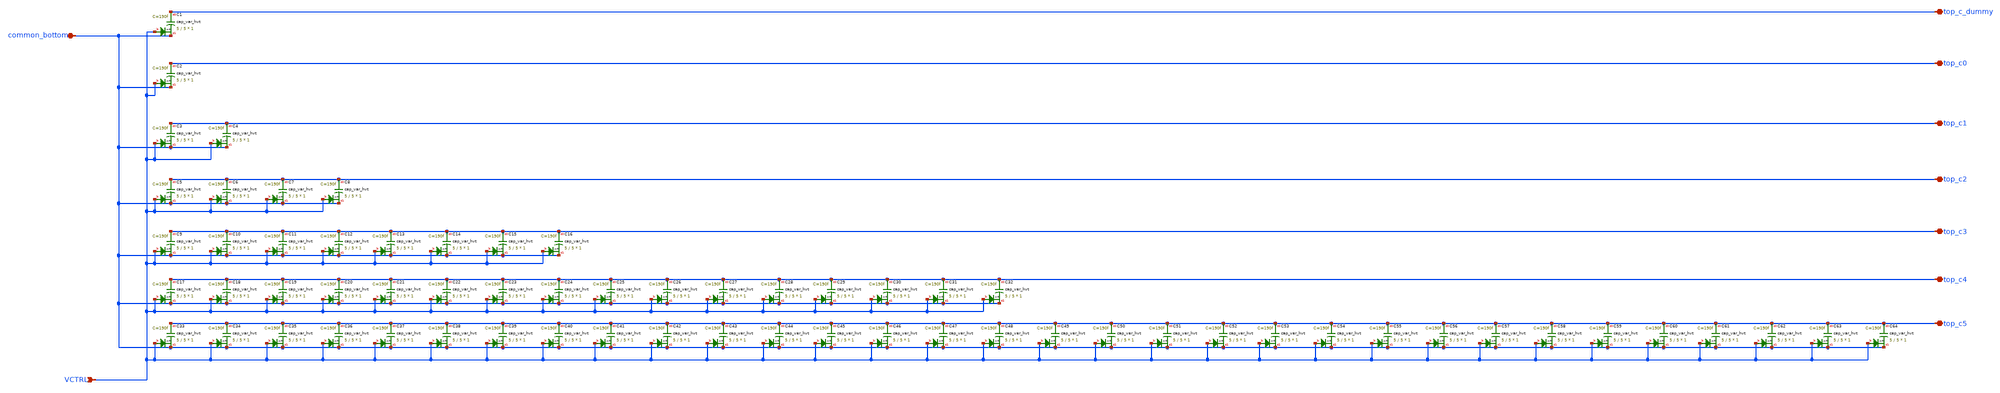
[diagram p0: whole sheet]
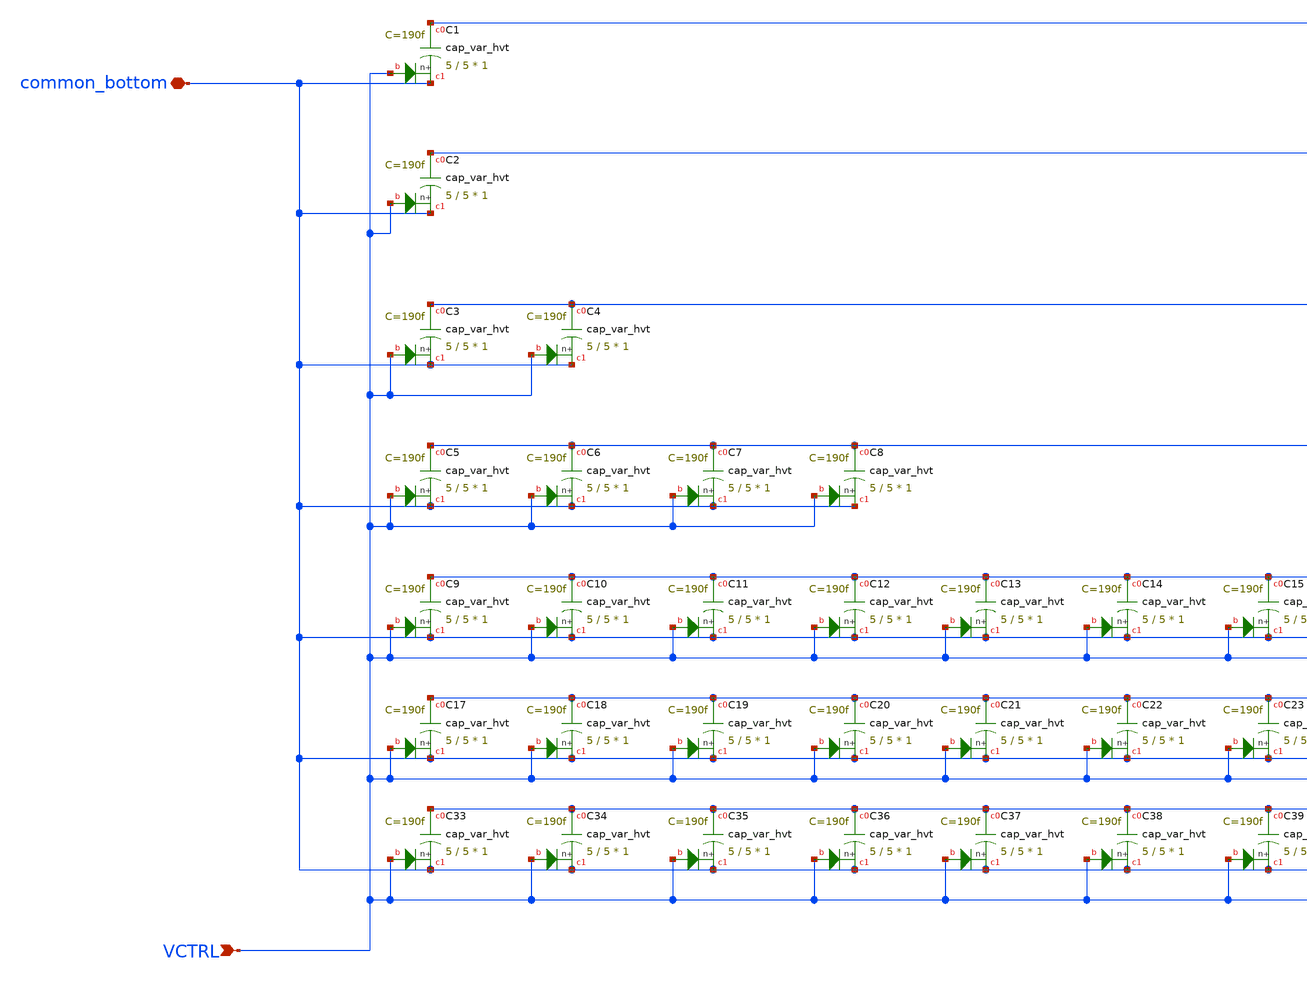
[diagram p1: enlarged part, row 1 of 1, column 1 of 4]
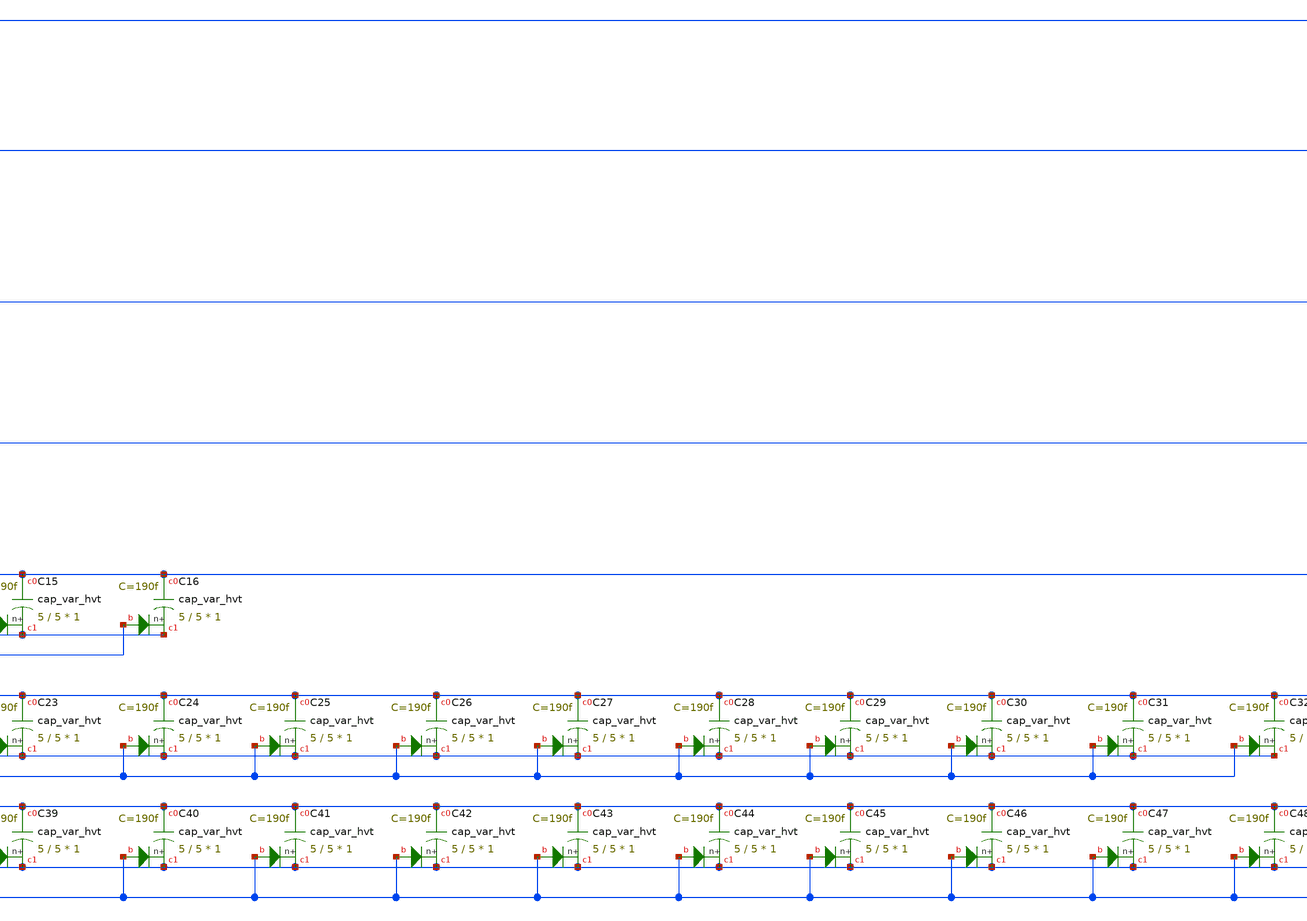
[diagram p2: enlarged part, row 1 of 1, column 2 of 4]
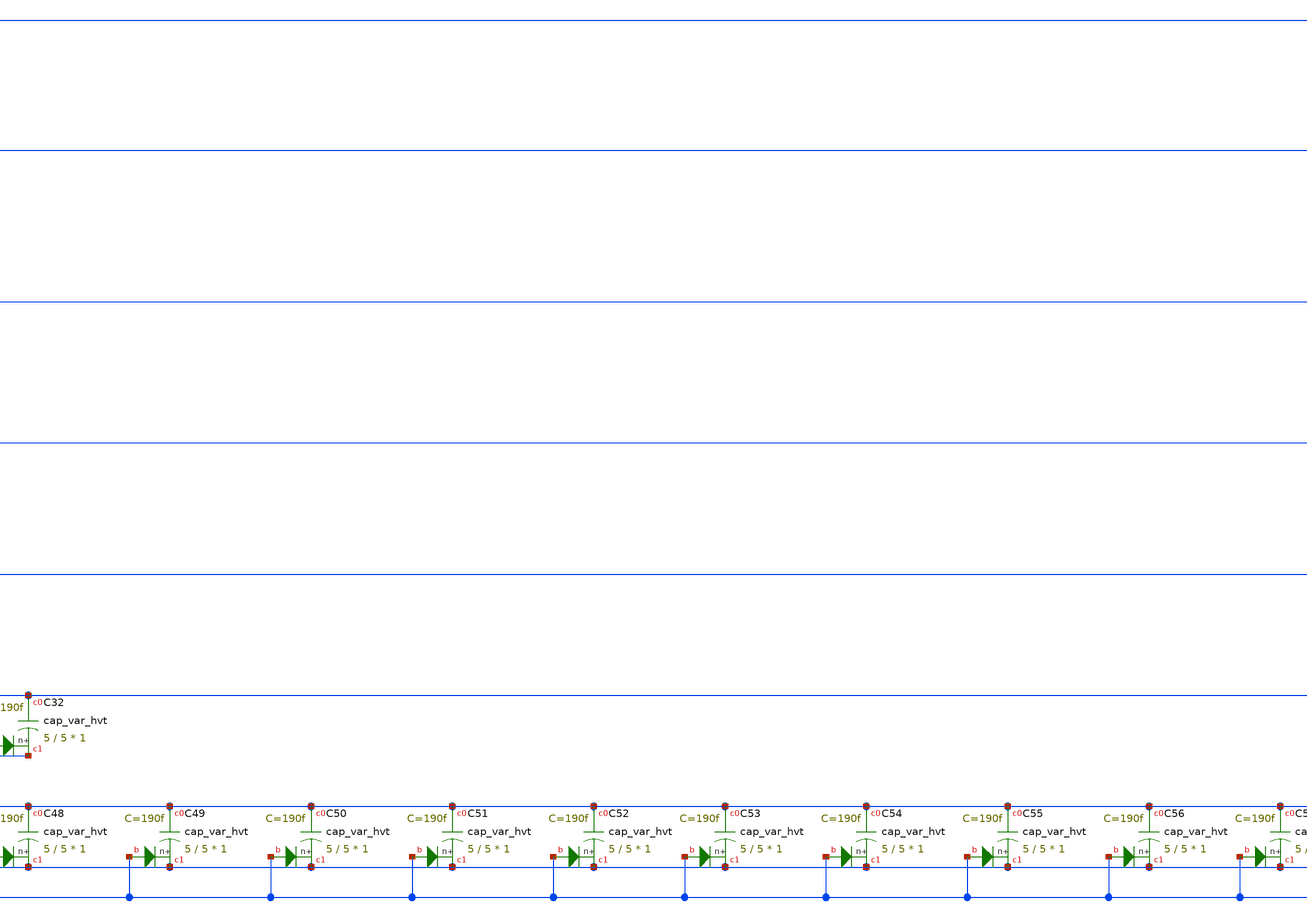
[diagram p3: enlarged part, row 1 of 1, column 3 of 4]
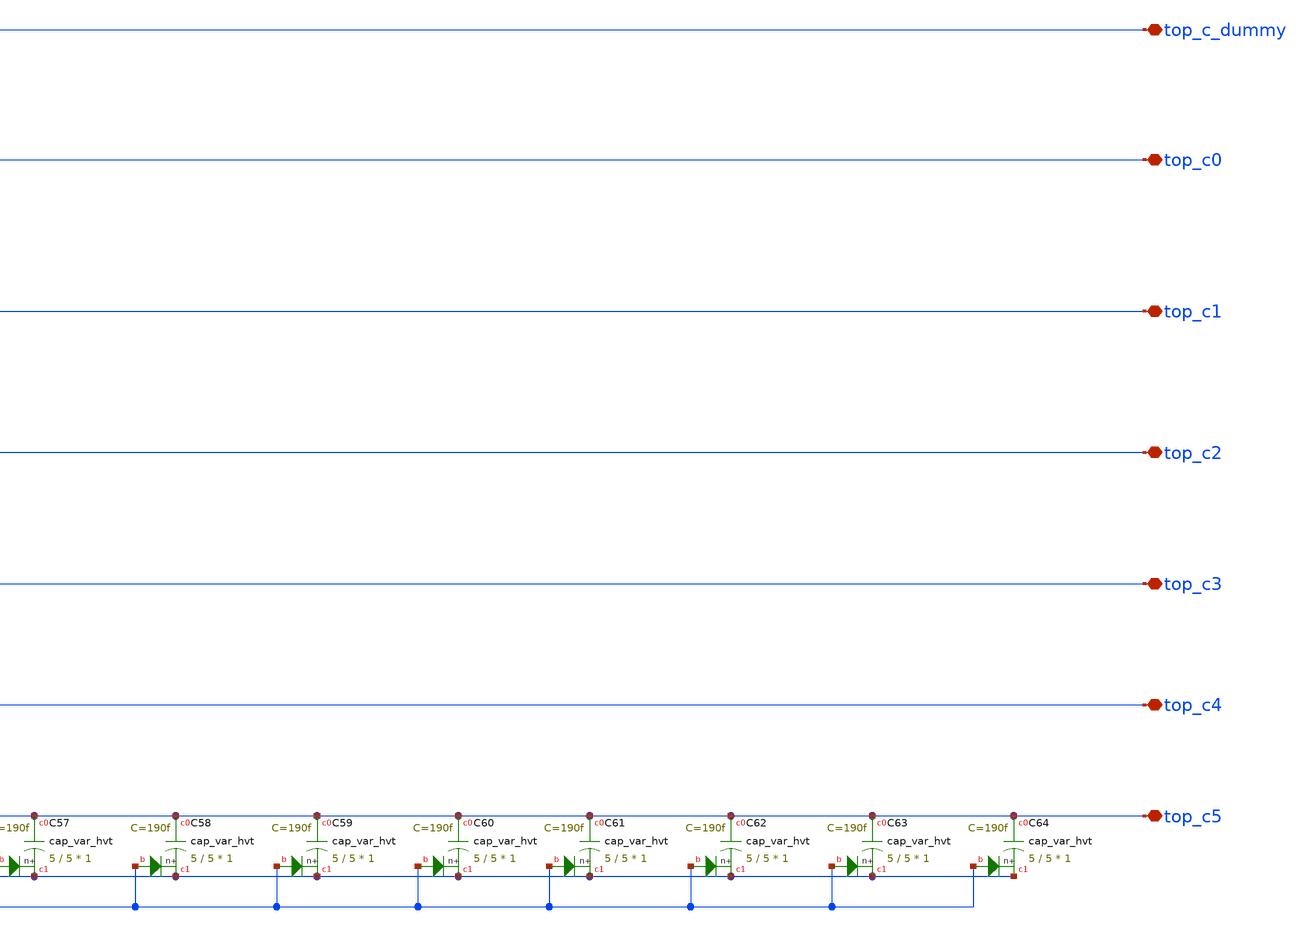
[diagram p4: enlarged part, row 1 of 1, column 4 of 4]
** sch_path: SKY130/SAR-ADC/SAR-ADC_5.0V/cap_array_var.sch
**.subckt cap_array_var common_bottom top_c_dummy top_c0 top_c5 top_c4 top_c3 top_c2 top_c1 VCTRL
*.iopin common_bottom
*.iopin top_c_dummy
*.iopin top_c0
*.iopin top_c5
*.iopin top_c4
*.iopin top_c3
*.iopin top_c2
*.iopin top_c1
*.ipin VCTRL
XC1 top_c_dummy common_bottom VCTRL sky130_fd_pr__cap_var_hvt W=5 L=5 VM=1 m=1
XC2 top_c0 common_bottom VCTRL sky130_fd_pr__cap_var_hvt W=5 L=5 VM=1 m=1
XC3 top_c1 common_bottom VCTRL sky130_fd_pr__cap_var_hvt W=5 L=5 VM=1 m=1
XC4 top_c1 common_bottom VCTRL sky130_fd_pr__cap_var_hvt W=5 L=5 VM=1 m=1
XC5 top_c2 common_bottom VCTRL sky130_fd_pr__cap_var_hvt W=5 L=5 VM=1 m=1
XC6 top_c2 common_bottom VCTRL sky130_fd_pr__cap_var_hvt W=5 L=5 VM=1 m=1
XC7 top_c2 common_bottom VCTRL sky130_fd_pr__cap_var_hvt W=5 L=5 VM=1 m=1
XC8 top_c2 common_bottom VCTRL sky130_fd_pr__cap_var_hvt W=5 L=5 VM=1 m=1
XC9 top_c3 common_bottom VCTRL sky130_fd_pr__cap_var_hvt W=5 L=5 VM=1 m=1
XC10 top_c3 common_bottom VCTRL sky130_fd_pr__cap_var_hvt W=5 L=5 VM=1 m=1
XC11 top_c3 common_bottom VCTRL sky130_fd_pr__cap_var_hvt W=5 L=5 VM=1 m=1
XC12 top_c3 common_bottom VCTRL sky130_fd_pr__cap_var_hvt W=5 L=5 VM=1 m=1
XC13 top_c3 common_bottom VCTRL sky130_fd_pr__cap_var_hvt W=5 L=5 VM=1 m=1
XC14 top_c3 common_bottom VCTRL sky130_fd_pr__cap_var_hvt W=5 L=5 VM=1 m=1
XC15 top_c3 common_bottom VCTRL sky130_fd_pr__cap_var_hvt W=5 L=5 VM=1 m=1
XC16 top_c3 common_bottom VCTRL sky130_fd_pr__cap_var_hvt W=5 L=5 VM=1 m=1
XC17 top_c4 common_bottom VCTRL sky130_fd_pr__cap_var_hvt W=5 L=5 VM=1 m=1
XC18 top_c4 common_bottom VCTRL sky130_fd_pr__cap_var_hvt W=5 L=5 VM=1 m=1
XC19 top_c4 common_bottom VCTRL sky130_fd_pr__cap_var_hvt W=5 L=5 VM=1 m=1
XC20 top_c4 common_bottom VCTRL sky130_fd_pr__cap_var_hvt W=5 L=5 VM=1 m=1
XC21 top_c4 common_bottom VCTRL sky130_fd_pr__cap_var_hvt W=5 L=5 VM=1 m=1
XC22 top_c4 common_bottom VCTRL sky130_fd_pr__cap_var_hvt W=5 L=5 VM=1 m=1
XC23 top_c4 common_bottom VCTRL sky130_fd_pr__cap_var_hvt W=5 L=5 VM=1 m=1
XC24 top_c4 common_bottom VCTRL sky130_fd_pr__cap_var_hvt W=5 L=5 VM=1 m=1
XC25 top_c4 common_bottom VCTRL sky130_fd_pr__cap_var_hvt W=5 L=5 VM=1 m=1
XC26 top_c4 common_bottom VCTRL sky130_fd_pr__cap_var_hvt W=5 L=5 VM=1 m=1
XC27 top_c4 common_bottom VCTRL sky130_fd_pr__cap_var_hvt W=5 L=5 VM=1 m=1
XC28 top_c4 common_bottom VCTRL sky130_fd_pr__cap_var_hvt W=5 L=5 VM=1 m=1
XC29 top_c4 common_bottom VCTRL sky130_fd_pr__cap_var_hvt W=5 L=5 VM=1 m=1
XC30 top_c4 common_bottom VCTRL sky130_fd_pr__cap_var_hvt W=5 L=5 VM=1 m=1
XC31 top_c4 common_bottom VCTRL sky130_fd_pr__cap_var_hvt W=5 L=5 VM=1 m=1
XC32 top_c4 common_bottom VCTRL sky130_fd_pr__cap_var_hvt W=5 L=5 VM=1 m=1
XC33 top_c5 common_bottom VCTRL sky130_fd_pr__cap_var_hvt W=5 L=5 VM=1 m=1
XC34 top_c5 common_bottom VCTRL sky130_fd_pr__cap_var_hvt W=5 L=5 VM=1 m=1
XC35 top_c5 common_bottom VCTRL sky130_fd_pr__cap_var_hvt W=5 L=5 VM=1 m=1
XC36 top_c5 common_bottom VCTRL sky130_fd_pr__cap_var_hvt W=5 L=5 VM=1 m=1
XC37 top_c5 common_bottom VCTRL sky130_fd_pr__cap_var_hvt W=5 L=5 VM=1 m=1
XC38 top_c5 common_bottom VCTRL sky130_fd_pr__cap_var_hvt W=5 L=5 VM=1 m=1
XC39 top_c5 common_bottom VCTRL sky130_fd_pr__cap_var_hvt W=5 L=5 VM=1 m=1
XC40 top_c5 common_bottom VCTRL sky130_fd_pr__cap_var_hvt W=5 L=5 VM=1 m=1
XC41 top_c5 common_bottom VCTRL sky130_fd_pr__cap_var_hvt W=5 L=5 VM=1 m=1
XC42 top_c5 common_bottom VCTRL sky130_fd_pr__cap_var_hvt W=5 L=5 VM=1 m=1
XC43 top_c5 common_bottom VCTRL sky130_fd_pr__cap_var_hvt W=5 L=5 VM=1 m=1
XC44 top_c5 common_bottom VCTRL sky130_fd_pr__cap_var_hvt W=5 L=5 VM=1 m=1
XC45 top_c5 common_bottom VCTRL sky130_fd_pr__cap_var_hvt W=5 L=5 VM=1 m=1
XC46 top_c5 common_bottom VCTRL sky130_fd_pr__cap_var_hvt W=5 L=5 VM=1 m=1
XC47 top_c5 common_bottom VCTRL sky130_fd_pr__cap_var_hvt W=5 L=5 VM=1 m=1
XC48 top_c5 common_bottom VCTRL sky130_fd_pr__cap_var_hvt W=5 L=5 VM=1 m=1
XC49 top_c5 common_bottom VCTRL sky130_fd_pr__cap_var_hvt W=5 L=5 VM=1 m=1
XC50 top_c5 common_bottom VCTRL sky130_fd_pr__cap_var_hvt W=5 L=5 VM=1 m=1
XC51 top_c5 common_bottom VCTRL sky130_fd_pr__cap_var_hvt W=5 L=5 VM=1 m=1
XC52 top_c5 common_bottom VCTRL sky130_fd_pr__cap_var_hvt W=5 L=5 VM=1 m=1
XC53 top_c5 common_bottom VCTRL sky130_fd_pr__cap_var_hvt W=5 L=5 VM=1 m=1
XC54 top_c5 common_bottom VCTRL sky130_fd_pr__cap_var_hvt W=5 L=5 VM=1 m=1
XC55 top_c5 common_bottom VCTRL sky130_fd_pr__cap_var_hvt W=5 L=5 VM=1 m=1
XC56 top_c5 common_bottom VCTRL sky130_fd_pr__cap_var_hvt W=5 L=5 VM=1 m=1
XC57 top_c5 common_bottom VCTRL sky130_fd_pr__cap_var_hvt W=5 L=5 VM=1 m=1
XC58 top_c5 common_bottom VCTRL sky130_fd_pr__cap_var_hvt W=5 L=5 VM=1 m=1
XC59 top_c5 common_bottom VCTRL sky130_fd_pr__cap_var_hvt W=5 L=5 VM=1 m=1
XC60 top_c5 common_bottom VCTRL sky130_fd_pr__cap_var_hvt W=5 L=5 VM=1 m=1
XC61 top_c5 common_bottom VCTRL sky130_fd_pr__cap_var_hvt W=5 L=5 VM=1 m=1
XC62 top_c5 common_bottom VCTRL sky130_fd_pr__cap_var_hvt W=5 L=5 VM=1 m=1
XC63 top_c5 common_bottom VCTRL sky130_fd_pr__cap_var_hvt W=5 L=5 VM=1 m=1
XC64 top_c5 common_bottom VCTRL sky130_fd_pr__cap_var_hvt W=5 L=5 VM=1 m=1
**.ends
.end
